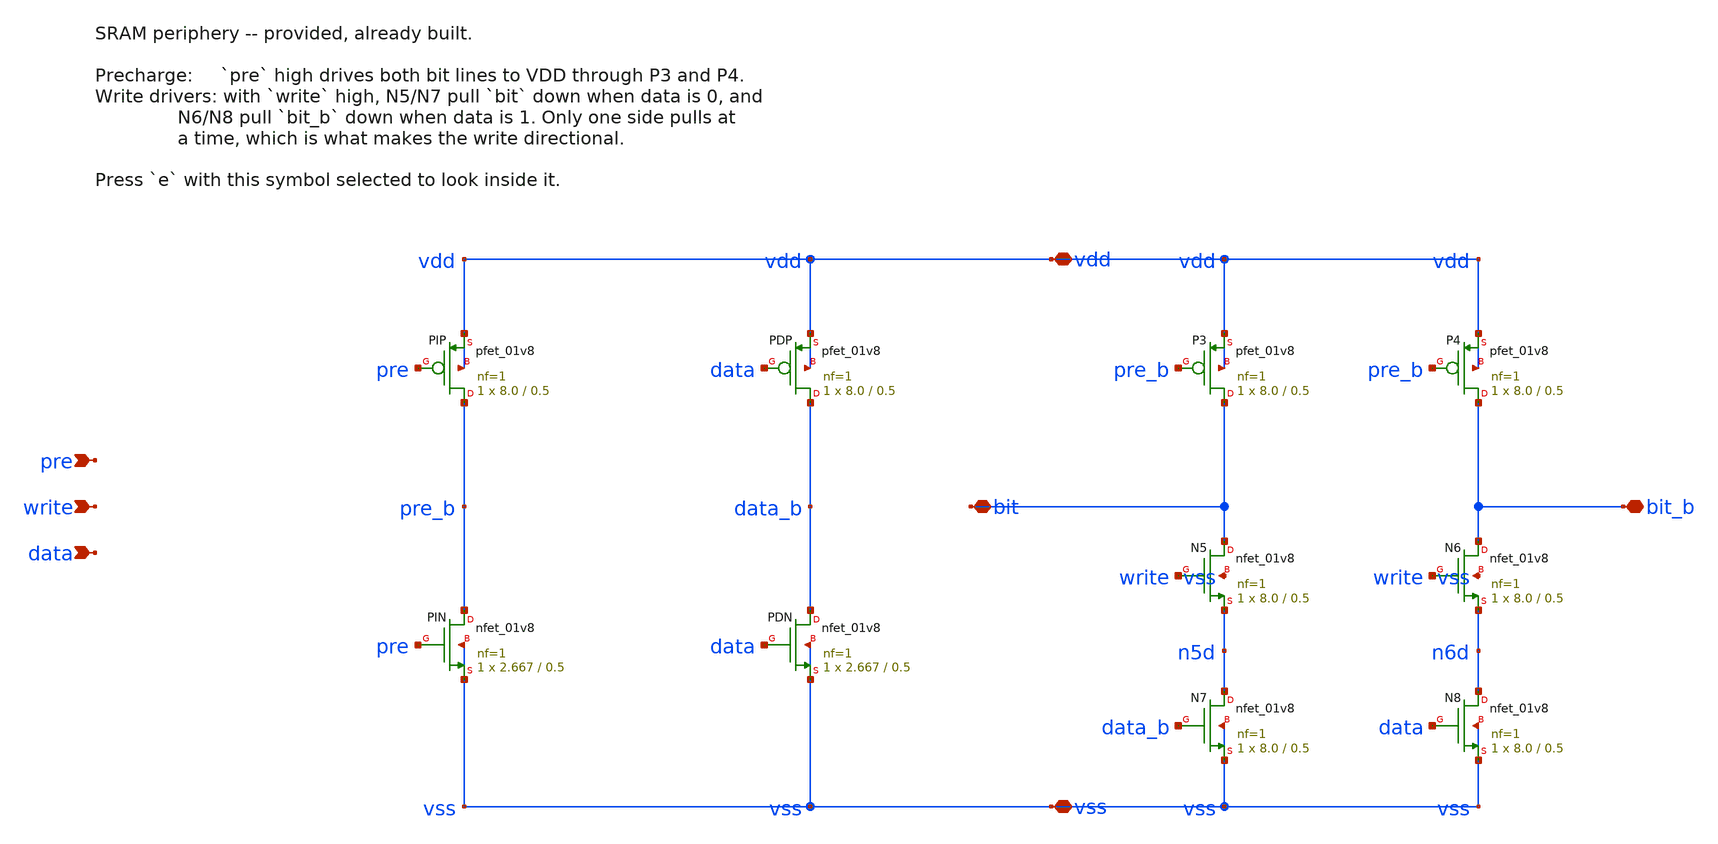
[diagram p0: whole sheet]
** sch_path: lab4_sram/xschem/sram_periph.sch
**.subckt sram_periph pre write data bit bit_b vdd vss
*.ipin pre
*.ipin write
*.ipin data
*.iopin bit
*.iopin bit_b
*.iopin vdd
*.iopin vss
XPIP pre_b pre vdd vdd sky130_fd_pr__pfet_01v8 L=0.5 W=8.0 nf=1 ad='int((nf+1)/2) * W/nf * 0.29' as='int((nf+2)/2) * W/nf * 0.29'
+ pd='2*int((nf+1)/2) * (W/nf + 0.29)' ps='2*int((nf+2)/2) * (W/nf + 0.29)' nrd='0.29 / W' nrs='0.29 / W'
+ sa=0 sb=0 sd=0 mult=1 m=1
XPIN pre_b pre vss vss sky130_fd_pr__nfet_01v8 L=0.5 W=2.667 nf=1 ad='int((1 + 1)/2) * 2.667 / 1 * 0.29'
+ as='int((1 + 2)/2) * 2.667 / 1 * 0.29' pd='2*int((1 + 1)/2) * (2.667 / 1 + 0.29)' ps='2*int((1 + 2)/2) * (2.667 / 1 + 0.29)'
+ nrd='0.29 / 2.667 ' nrs='0.29 / 2.667 ' sa=0 sb=0 sd=0 mult=1 m=1
XPDP data_b data vdd vdd sky130_fd_pr__pfet_01v8 L=0.5 W=8.0 nf=1 ad='int((nf+1)/2) * W/nf * 0.29' as='int((nf+2)/2) * W/nf * 0.29'
+ pd='2*int((nf+1)/2) * (W/nf + 0.29)' ps='2*int((nf+2)/2) * (W/nf + 0.29)' nrd='0.29 / W' nrs='0.29 / W'
+ sa=0 sb=0 sd=0 mult=1 m=1
XPDN data_b data vss vss sky130_fd_pr__nfet_01v8 L=0.5 W=2.667 nf=1 ad='int((1 + 1)/2) * 2.667 / 1 * 0.29'
+ as='int((1 + 2)/2) * 2.667 / 1 * 0.29' pd='2*int((1 + 1)/2) * (2.667 / 1 + 0.29)' ps='2*int((1 + 2)/2) * (2.667 / 1 + 0.29)'
+ nrd='0.29 / 2.667 ' nrs='0.29 / 2.667 ' sa=0 sb=0 sd=0 mult=1 m=1
XP3 bit pre_b vdd vdd sky130_fd_pr__pfet_01v8 L=0.5 W=8.0 nf=1 ad='int((nf+1)/2) * W/nf * 0.29' as='int((nf+2)/2) * W/nf * 0.29'
+ pd='2*int((nf+1)/2) * (W/nf + 0.29)' ps='2*int((nf+2)/2) * (W/nf + 0.29)' nrd='0.29 / W' nrs='0.29 / W'
+ sa=0 sb=0 sd=0 mult=1 m=1
XN5 bit write n5d vss sky130_fd_pr__nfet_01v8 L=0.5 W=8.0 nf=1 ad='int((1 + 1)/2) * 8.0 / 1 * 0.29' as='int((1 + 2)/2) * 8.0 / 1 * 0.29'
+ pd='2*int((1 + 1)/2) * (8.0 / 1 + 0.29)' ps='2*int((1 + 2)/2) * (8.0 / 1 + 0.29)' nrd='0.29 / 8.0 ' nrs='0.29 / 8.0 '
+ sa=0 sb=0 sd=0 mult=1 m=1
XN7 n5d data_b vss vss sky130_fd_pr__nfet_01v8 L=0.5 W=8.0 nf=1 ad='int((1 + 1)/2) * 8.0 / 1 * 0.29'
+ as='int((1 + 2)/2) * 8.0 / 1 * 0.29' pd='2*int((1 + 1)/2) * (8.0 / 1 + 0.29)' ps='2*int((1 + 2)/2) * (8.0 / 1 + 0.29)'
+ nrd='0.29 / 8.0 ' nrs='0.29 / 8.0 ' sa=0 sb=0 sd=0 mult=1 m=1
XP4 bit_b pre_b vdd vdd sky130_fd_pr__pfet_01v8 L=0.5 W=8.0 nf=1 ad='int((nf+1)/2) * W/nf * 0.29' as='int((nf+2)/2) * W/nf * 0.29'
+ pd='2*int((nf+1)/2) * (W/nf + 0.29)' ps='2*int((nf+2)/2) * (W/nf + 0.29)' nrd='0.29 / W' nrs='0.29 / W'
+ sa=0 sb=0 sd=0 mult=1 m=1
XN6 bit_b write n6d vss sky130_fd_pr__nfet_01v8 L=0.5 W=8.0 nf=1 ad='int((1 + 1)/2) * 8.0 / 1 * 0.29'
+ as='int((1 + 2)/2) * 8.0 / 1 * 0.29' pd='2*int((1 + 1)/2) * (8.0 / 1 + 0.29)' ps='2*int((1 + 2)/2) * (8.0 / 1 + 0.29)'
+ nrd='0.29 / 8.0 ' nrs='0.29 / 8.0 ' sa=0 sb=0 sd=0 mult=1 m=1
XN8 n6d data vss vss sky130_fd_pr__nfet_01v8 L=0.5 W=8.0 nf=1 ad='int((1 + 1)/2) * 8.0 / 1 * 0.29' as='int((1 + 2)/2) * 8.0 / 1 * 0.29'
+ pd='2*int((1 + 1)/2) * (8.0 / 1 + 0.29)' ps='2*int((1 + 2)/2) * (8.0 / 1 + 0.29)' nrd='0.29 / 8.0 ' nrs='0.29 / 8.0 '
+ sa=0 sb=0 sd=0 mult=1 m=1
**.ends
.end
